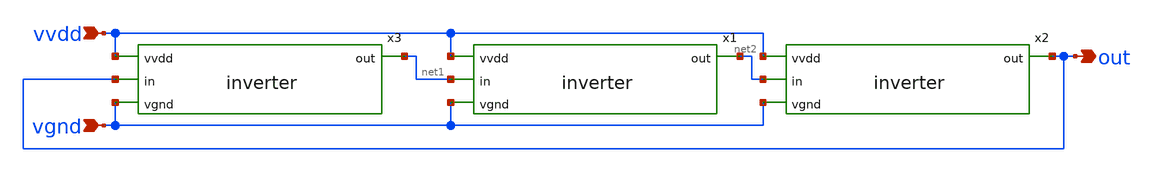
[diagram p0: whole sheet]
** sch_path: ring_oscillator/ring_oscillator.sch
**.subckt ring_oscillator vvdd vgnd out
*.ipin vvdd
*.ipin vgnd
*.opin out
x1 vvdd net1 net2 vgnd inverter
x2 vvdd net2 out vgnd inverter
x3 vvdd out net1 vgnd inverter
**.ends
.end
